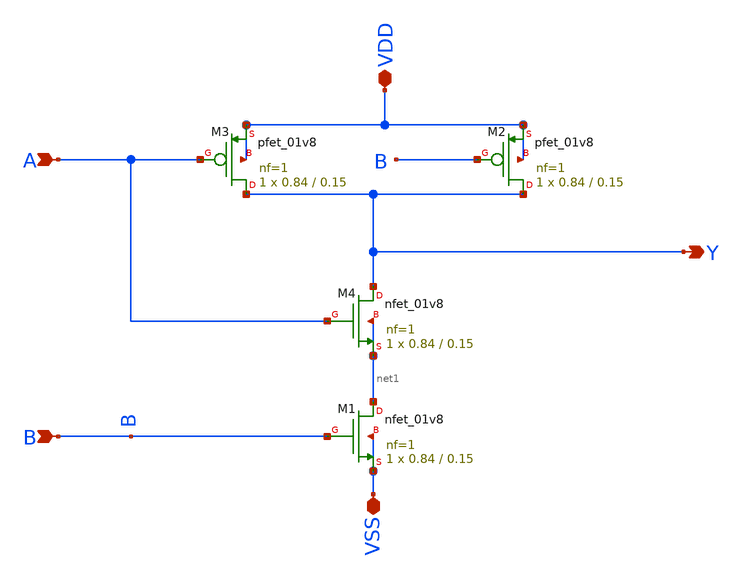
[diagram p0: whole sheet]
** sch_path: schematics/nand2.sch
**.subckt nand2 A B Y VDD VSS
*.ipin A
*.ipin B
*.opin Y
*.iopin VDD
*.iopin VSS
XM1 net1 B VSS VSS sky130_fd_pr__nfet_01v8 L=0.15 W=0.84 nf=1 ad='int((1 + 1)/2) * 0.84 / 1 * 0.29' as='int((1 + 2)/2) * 0.84 / 1 * 0.29'
+ pd='2*int((1 + 1)/2) * (0.84 / 1 + 0.29)' ps='2*int((1 + 2)/2) * (0.84 / 1 + 0.29)' nrd='0.29 / 0.84 '
+ nrs='0.29 / 0.84 ' sa=0 sb=0 sd=0 mult=1 m=1
XM2 Y B VDD VDD sky130_fd_pr__pfet_01v8 L=0.15 W=0.84 nf=1 ad='int((1 + 1)/2) * 0.84 / 1 * 0.29' as='int((1 + 2)/2) * 0.84 / 1 * 0.29'
+ pd='2*int((1 + 1)/2) * (0.84 / 1 + 0.29)' ps='2*int((1 + 2)/2) * (0.84 / 1 + 0.29)' nrd='0.29 / 0.84 '
+ nrs='0.29 / 0.84 ' sa=0 sb=0 sd=0 mult=1 m=1
XM3 Y A VDD VDD sky130_fd_pr__pfet_01v8 L=0.15 W=0.84 nf=1 ad='int((1 + 1)/2) * 0.84 / 1 * 0.29' as='int((1 + 2)/2) * 0.84 / 1 * 0.29'
+ pd='2*int((1 + 1)/2) * (0.84 / 1 + 0.29)' ps='2*int((1 + 2)/2) * (0.84 / 1 + 0.29)' nrd='0.29 / 0.84 '
+ nrs='0.29 / 0.84 ' sa=0 sb=0 sd=0 mult=1 m=1
XM4 Y A net1 net1 sky130_fd_pr__nfet_01v8 L=0.15 W=0.84 nf=1 ad='int((1 + 1)/2) * 0.84 / 1 * 0.29' as='int((1 + 2)/2) * 0.84 / 1 * 0.29'
+ pd='2*int((1 + 1)/2) * (0.84 / 1 + 0.29)' ps='2*int((1 + 2)/2) * (0.84 / 1 + 0.29)' nrd='0.29 / 0.84 '
+ nrs='0.29 / 0.84 ' sa=0 sb=0 sd=0 mult=1 m=1
**.ends
.end
